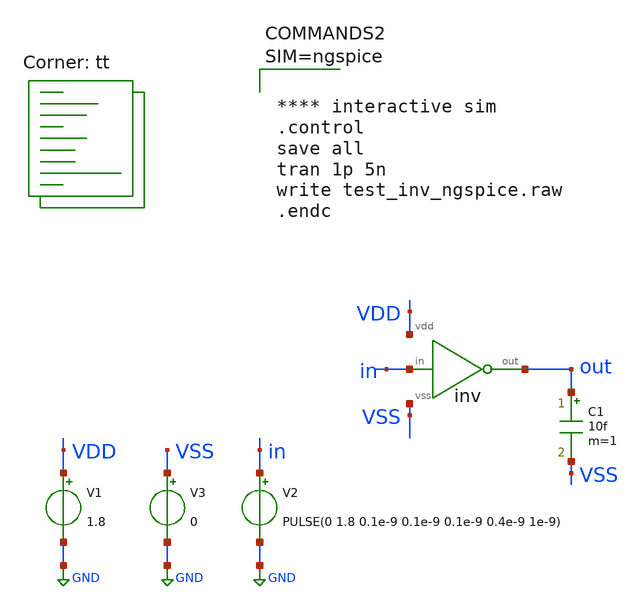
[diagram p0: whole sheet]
** sch_path: sample/xschem/tb_inv.sch
**.subckt tb_inv
x1 in out VDD VSS inv
C1 out VSS 10f m=1
V1 VDD GND 1.8
V3 VSS GND 0
V2 in GND PULSE(0 1.8 0.1e-9 0.1e-9 0.1e-9 0.4e-9 1e-9)
**** begin user architecture code



**** interactive sim
.control
save all
tran 1p 5n
write test_inv_ngspice.raw
.endc



.lib $::SKYWATER_MODELS/sky130.lib.spice tt
**** end user architecture code
**.ends

* expanding   symbol:  inv.sym # of pins=4
** sym_path: sample/xschem/inv.sym
** sch_path: sample/xschem/inv.sch
.subckt inv in out vdd vss
*.iopin vdd
*.ipin in
*.opin out
*.iopin vss
XM1 out in vss vss sky130_fd_pr__nfet_01v8 L=0.15 W=0.65 nf=1 ad='int((nf+1)/2) * W/nf * 0.29' as='int((nf+2)/2) * W/nf * 0.29'
+ pd='2*int((nf+1)/2) * (W/nf + 0.29)' ps='2*int((nf+2)/2) * (W/nf + 0.29)' nrd='0.29 / W' nrs='0.29 / W'
+ sa=0 sb=0 sd=0 mult=1 m=1
XM8 out in vdd vdd sky130_fd_pr__pfet_01v8_hvt L=0.15 W=1 nf=1 ad='int((1 + 1)/2) * 1 / 1 * 0.29' as='int((1 + 2)/2) * 1 / 1 * 0.29'
+ pd='2*int((1 + 1)/2) * (1 / 1 + 0.29)' ps='2*int((1 + 2)/2) * (1 / 1 + 0.29)' nrd='0.29 / 1 ' nrs='0.29 / 1 '
+ sa=0 sb=0 sd=0 mult=1 m=1
.ends

.GLOBAL GND
.end
